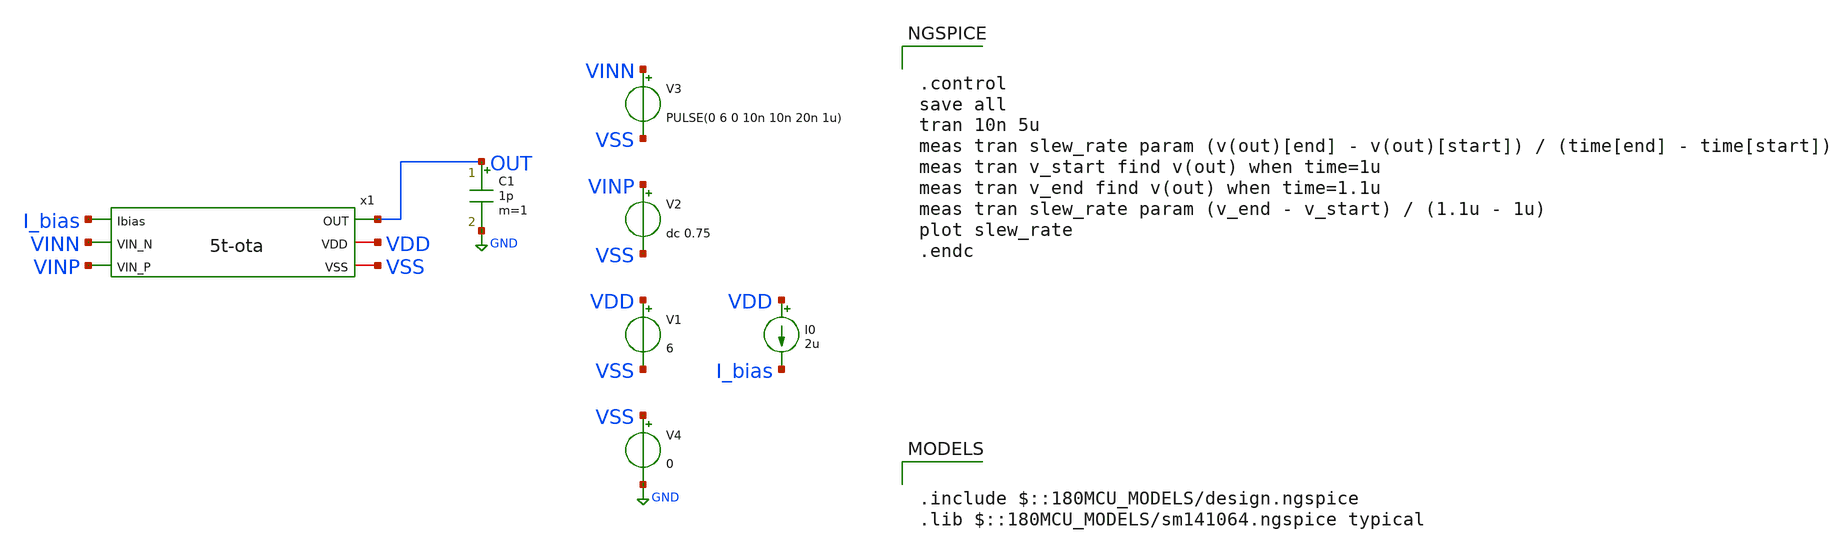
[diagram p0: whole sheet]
** sch_path: week02_current_diffpair/tugas5_cascode_current_mirror/5t-ota-slew-rate.sch
**.subckt 5t-ota-slew-rate
V1 VDD VSS 6
V2 VINP VSS dc 0.75
V3 VINN VSS PULSE(0 6 0 10n 10n 20n 1u)
V4 VSS GND 0
I0 VDD I_bias 2u
x1 I_bias VINN VINP OUT VDD VSS 5t-ota
C1 OUT GND 1p m=1
**** begin user architecture code

.include $::180MCU_MODELS/design.ngspice
.lib $::180MCU_MODELS/sm141064.ngspice typical



.control
save all
tran 10n 5u
meas tran slew_rate param (v(out)[end] - v(out)[start]) / (time[end] - time[start])
meas tran v_start find v(out) when time=1u
meas tran v_end find v(out) when time=1.1u
meas tran slew_rate param (v_end - v_start) / (1.1u - 1u)
plot slew_rate
.endc


**** end user architecture code
**.ends

* expanding   symbol:  5t-ota.sym # of pins=6
** sym_path: week02_current_diffpair/tugas5_cascode_current_mirror/5t-ota.sym
** sch_path: week02_current_diffpair/tugas5_cascode_current_mirror/5t-ota.sch
.subckt 5t-ota Ibias VIN_N VIN_P OUT VDD VSS
*.ipin VIN_N
*.ipin VIN_P
*.opin OUT
*.iopin VDD
*.iopin VSS
*.ipin Ibias
XM4 net1 Ibias VSS VSS nfet_06v0 L=1u W=2.5u nf=1 ad='int((nf+1)/2) * W/nf * 0.18u' as='int((nf+2)/2) * W/nf * 0.18u'
+ pd='2*int((nf+1)/2) * (W/nf + 0.18u)' ps='2*int((nf+2)/2) * (W/nf + 0.18u)' nrd='0.18u / W' nrs='0.18u / W'
+ sa=0 sb=0 sd=0 m=1
XM8 Ibias Ibias VSS VSS nfet_06v0 L=1u W=5u nf=1 ad='int((nf+1)/2) * W/nf * 0.18u' as='int((nf+2)/2) * W/nf * 0.18u'
+ pd='2*int((nf+1)/2) * (W/nf + 0.18u)' ps='2*int((nf+2)/2) * (W/nf + 0.18u)' nrd='0.18u / W' nrs='0.18u / W'
+ sa=0 sb=0 sd=0 m=1
XM9 net2 net2 VDD VDD pfet_06v0 L=1u W=5u nf=1 ad='int((nf+1)/2) * W/nf * 0.18u' as='int((nf+2)/2) * W/nf * 0.18u'
+ pd='2*int((nf+1)/2) * (W/nf + 0.18u)' ps='2*int((nf+2)/2) * (W/nf + 0.18u)' nrd='0.18u / W' nrs='0.18u / W'
+ sa=0 sb=0 sd=0 m=1
XM10 OUT VIN_P net1 VSS nfet_06v0 L=1u W=20u nf=1 ad='int((nf+1)/2) * W/nf * 0.18u' as='int((nf+2)/2) * W/nf * 0.18u'
+ pd='2*int((nf+1)/2) * (W/nf + 0.18u)' ps='2*int((nf+2)/2) * (W/nf + 0.18u)' nrd='0.18u / W' nrs='0.18u / W'
+ sa=0 sb=0 sd=0 m=1
XM11 net2 VIN_N net1 VSS nfet_06v0 L=1u W=20u nf=1 ad='int((nf+1)/2) * W/nf * 0.18u' as='int((nf+2)/2) * W/nf * 0.18u'
+ pd='2*int((nf+1)/2) * (W/nf + 0.18u)' ps='2*int((nf+2)/2) * (W/nf + 0.18u)' nrd='0.18u / W' nrs='0.18u / W'
+ sa=0 sb=0 sd=0 m=1
XM12 OUT net2 VDD VDD pfet_06v0 L=1u W=5u nf=1 ad='int((nf+1)/2) * W/nf * 0.18u' as='int((nf+2)/2) * W/nf * 0.18u'
+ pd='2*int((nf+1)/2) * (W/nf + 0.18u)' ps='2*int((nf+2)/2) * (W/nf + 0.18u)' nrd='0.18u / W' nrs='0.18u / W'
+ sa=0 sb=0 sd=0 m=1
.ends

.GLOBAL GND
.end
